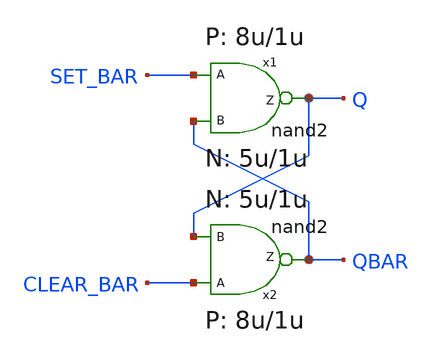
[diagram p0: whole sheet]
** sch_path: xschem_library/examples/test.sch
**.subckt test
x1 Q SET_BAR QBAR nand2 W_P=8u L_P=1u W_N=5u L_N=1u
x2 QBAR CLEAR_BAR Q nand2 W_P=8u L_P=1u W_N=5u L_N=1u
**.ends

* expanding   symbol:  nand2.sym # of pins=3
** sym_path: xschem_library/examples/nand2.sym
** sch_path: xschem_library/examples/nand2.sch
.subckt nand2 Z A B  W_P=8u L_P=1u W_N=5u L_N=1u
*.ipin A
*.opin Z
*.ipin B
m1 Z A net1 VSS nmos w=WN l=LN m=1
m2 Z B VCC VCC pmos w=WP l=LP m=1
m3 Z A VCC VCC pmos w=WP l=LP m=1
m4 net1 B VSS VSS nmos w=WN l=LN m=1
.ends

.GLOBAL VCC
.GLOBAL VSS
.end
